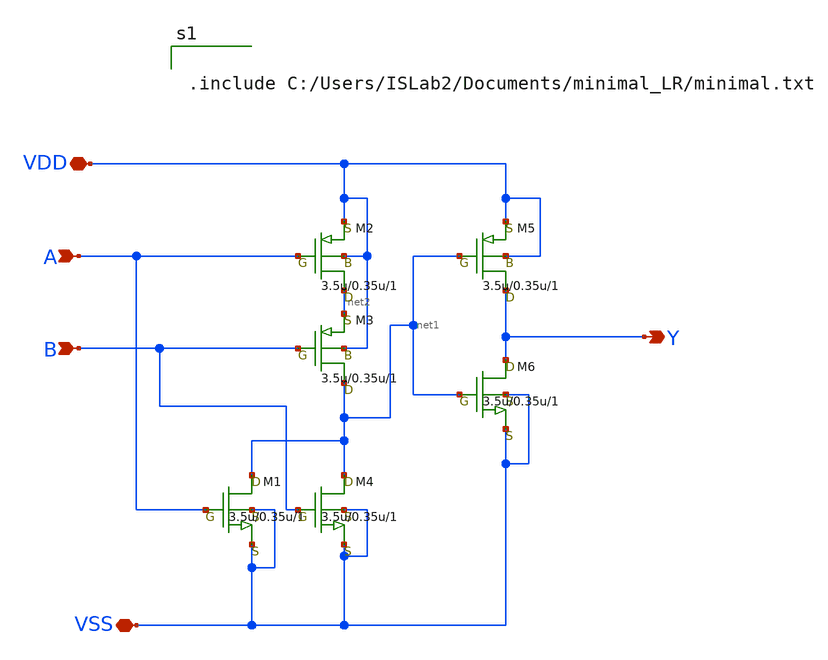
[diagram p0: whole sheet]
** sch_path: OR.sch
**.subckt OR VDD A B VSS Y
*.iopin VDD
*.ipin A
*.ipin B
*.iopin VSS
*.opin Y
M1 net1 A VSS VSS nch w=3.5u l=0.35u as=0 ps=0 ad=0 pd=0 m=1
M2 net2 A VDD VDD pch w=3.5u l=0.35u as=0 ps=0 ad=0 pd=0 m=1
M3 net1 B net2 VDD pch w=3.5u l=0.35u as=0 ps=0 ad=0 pd=0 m=1
M4 net1 B VSS VSS nch w=3.5u l=0.35u as=0 ps=0 ad=0 pd=0 m=1
M5 Y net1 VDD VDD pch w=3.5u l=0.35u as=0 ps=0 ad=0 pd=0 m=1
M6 Y net1 VSS VSS nch w=3.5u l=0.35u as=0 ps=0 ad=0 pd=0 m=1
**** begin user architecture code


.include C:/Users/ISLab2/Documents/minimal_LR/minimal.txt

**** end user architecture code
**.ends
.end
